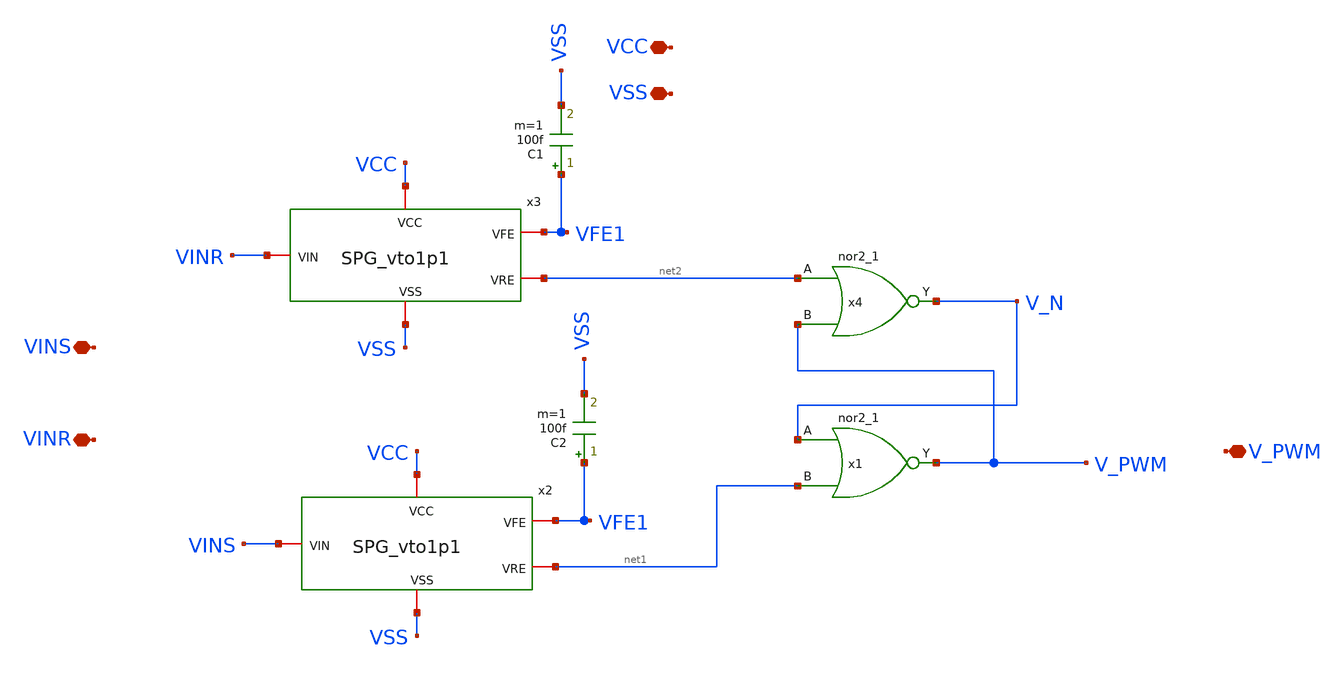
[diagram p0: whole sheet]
** sch_path: xschem/gf180_digital/PD/PD_vto1p1.sch
**.subckt PD_vto1p1 V_PWM VCC VSS VINS VINR
*.iopin V_PWM
*.iopin VCC
*.iopin VSS
*.iopin VINS
*.iopin VINR
C2 VFE1 VSS 100f m=1
C1 VFE1 VSS 100f m=1
x1 V_N net1 VSS VCC VSS VCC V_PWM gf180mcu_fd_sc_mcu9t5v0__nor2_1
x3 VCC VSS VFE1 VINR net2 SPG_vto1p1
x2 VCC VSS VFE1 VINS net1 SPG_vto1p1
x4 net2 V_PWM VSS VCC VSS VCC V_N gf180mcu_fd_sc_mcu9t5v0__nor2_1
**.ends

* expanding   symbol:  gf180_digital/SPG/SPG_vto1p1.sym # of pins=5
** sym_path: xschem/gf180_digital/SPG/SPG_vto1p1.sym
** sch_path: xschem/gf180_digital/SPG/SPG_vto1p1.sch
.subckt SPG_vto1p1 VDDd VSSd VFE VIN VRE
*.iopin VIN
*.iopin VFE
*.iopin VRE
*.iopin VDDd
*.iopin VSSd
x2 predly VSSd VDDd VSSd VDDd net2 gf180mcu_fd_sc_mcu9t5v0__inv_1
x3 vinn VSSd VDDd VSSd VDDd predly gf180mcu_fd_sc_mcu9t5v0__inv_1
x4 dly8 VSSd VDDd VSSd VDDd net1 gf180mcu_fd_sc_mcu9t5v0__inv_1
x5 VIN VSSd VDDd VSSd VDDd vinn gf180mcu_fd_sc_mcu9t5v0__inv_2
x6 predly VSSd VDDd VSSd VDDd V_gatein gf180mcu_fd_sc_mcu9t5v0__inv_8
x9 VDDd VSSd V_gatein dly7 large_delay_vto1p1
x1 dly7 VSSd VDDd VSSd VDDd dly8 gf180mcu_fd_sc_mcu9t5v0__inv_8
x8 net2 dly8 VFE VDDd VDDd VSSd VSSd gf180mcu_fd_sc_mcu9t5v0__and2_1
x7 net1 predly VRE VDDd VDDd VSSd VSSd gf180mcu_fd_sc_mcu9t5v0__and2_1
.ends


* expanding   symbol:  gf180_digital/large_delay/large_delay_vto1p1.sym # of pins=4
** sym_path: xschem/gf180_digital/large_delay/large_delay_vto1p1.sym
** sch_path: xschem/gf180_digital/large_delay/large_delay_vto1p1.sch
.subckt large_delay_vto1p1 VDDd VSSd VIN VOUT
*.iopin VIN
*.iopin VOUT
*.iopin VDDd
*.iopin VSSd
x1 VIN VOUT VDDd VDDd VSSd VSSd gf180mcu_fd_sc_mcu9t5v0__dlya_1
.ends

.end
